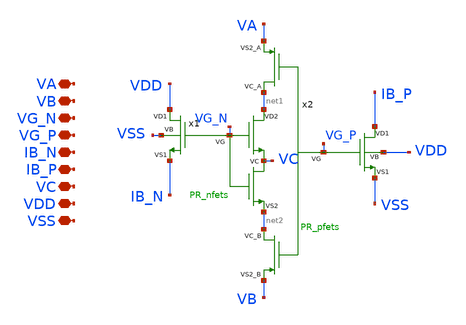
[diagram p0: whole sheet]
** sch_path: TIA/xschem/PseudoResistor/PR_net.sch
**.subckt PR_net VA VB VG_N VG_P IB_N IB_P VC VDD VSS
*.iopin VA
*.iopin VB
*.iopin VG_N
*.iopin VG_P
*.iopin IB_N
*.iopin IB_P
*.iopin VC
*.iopin VDD
*.iopin VSS
x1 VDD net1 IB_N net2 VG_N VC VSS PR_nfets
x2 IB_P VSS VA VB VG_P net1 net2 VDD PR_pfets
**.ends

* expanding   symbol:  /home/gmaranhao/Desktop/gf180_work/TIA/PseudoResistor/PR_nfets.sym # of
*+ pins=7
** sym_path: TIA/xschem/PseudoResistor/PR_nfets.sym
** sch_path: TIA/xschem/PseudoResistor/PR_nfets.sch
.subckt PR_nfets VD1 VD2 VS1 VS2 VG VC VB
*.iopin VD1
*.iopin VD2
*.iopin VS1
*.iopin VS2
*.iopin VG
*.iopin VC
*.iopin VB
XM5 VB VB VB VB nfet_03v3 L=2u W=2u nf=1 ad='int((nf+1)/2) * W/nf * 0.18u' as='int((nf+2)/2) * W/nf * 0.18u'
+ pd='2*int((nf+1)/2) * (W/nf + 0.18u)' ps='2*int((nf+2)/2) * (W/nf + 0.18u)' nrd='0.18u / W' nrs='0.18u / W'
+ sa=0 sb=0 sd=0 m=32
XM3 VD2 VG net1 VB nfet_03v3 L=2u W=2u nf=1 ad='int((nf+1)/2) * W/nf * 0.18u' as='int((nf+2)/2) * W/nf * 0.18u'
+ pd='2*int((nf+1)/2) * (W/nf + 0.18u)' ps='2*int((nf+2)/2) * (W/nf + 0.18u)' nrd='0.18u / W' nrs='0.18u / W'
+ sa=0 sb=0 sd=0 m=1
XM4 net1 VG VC VB nfet_03v3 L=2u W=2u nf=1 ad='int((nf+1)/2) * W/nf * 0.18u' as='int((nf+2)/2) * W/nf * 0.18u'
+ pd='2*int((nf+1)/2) * (W/nf + 0.18u)' ps='2*int((nf+2)/2) * (W/nf + 0.18u)' nrd='0.18u / W' nrs='0.18u / W'
+ sa=0 sb=0 sd=0 m=1
XM6 VD2 VG net2 VB nfet_03v3 L=2u W=2u nf=1 ad='int((nf+1)/2) * W/nf * 0.18u' as='int((nf+2)/2) * W/nf * 0.18u'
+ pd='2*int((nf+1)/2) * (W/nf + 0.18u)' ps='2*int((nf+2)/2) * (W/nf + 0.18u)' nrd='0.18u / W' nrs='0.18u / W'
+ sa=0 sb=0 sd=0 m=1
XM8 net2 VG VC VB nfet_03v3 L=2u W=2u nf=1 ad='int((nf+1)/2) * W/nf * 0.18u' as='int((nf+2)/2) * W/nf * 0.18u'
+ pd='2*int((nf+1)/2) * (W/nf + 0.18u)' ps='2*int((nf+2)/2) * (W/nf + 0.18u)' nrd='0.18u / W' nrs='0.18u / W'
+ sa=0 sb=0 sd=0 m=1
XM1 VC VG net3 VB nfet_03v3 L=2u W=2u nf=1 ad='int((nf+1)/2) * W/nf * 0.18u' as='int((nf+2)/2) * W/nf * 0.18u'
+ pd='2*int((nf+1)/2) * (W/nf + 0.18u)' ps='2*int((nf+2)/2) * (W/nf + 0.18u)' nrd='0.18u / W' nrs='0.18u / W'
+ sa=0 sb=0 sd=0 m=1
XM9 net3 VG VS2 VB nfet_03v3 L=2u W=2u nf=1 ad='int((nf+1)/2) * W/nf * 0.18u' as='int((nf+2)/2) * W/nf * 0.18u'
+ pd='2*int((nf+1)/2) * (W/nf + 0.18u)' ps='2*int((nf+2)/2) * (W/nf + 0.18u)' nrd='0.18u / W' nrs='0.18u / W'
+ sa=0 sb=0 sd=0 m=1
XM10 VC VG net4 VB nfet_03v3 L=2u W=2u nf=1 ad='int((nf+1)/2) * W/nf * 0.18u' as='int((nf+2)/2) * W/nf * 0.18u'
+ pd='2*int((nf+1)/2) * (W/nf + 0.18u)' ps='2*int((nf+2)/2) * (W/nf + 0.18u)' nrd='0.18u / W' nrs='0.18u / W'
+ sa=0 sb=0 sd=0 m=1
XM11 net4 VG VS2 VB nfet_03v3 L=2u W=2u nf=1 ad='int((nf+1)/2) * W/nf * 0.18u' as='int((nf+2)/2) * W/nf * 0.18u'
+ pd='2*int((nf+1)/2) * (W/nf + 0.18u)' ps='2*int((nf+2)/2) * (W/nf + 0.18u)' nrd='0.18u / W' nrs='0.18u / W'
+ sa=0 sb=0 sd=0 m=1
XM2 VD1 VG net5 VB nfet_03v3 L=2u W=2u nf=1 ad='int((nf+1)/2) * W/nf * 0.18u' as='int((nf+2)/2) * W/nf * 0.18u'
+ pd='2*int((nf+1)/2) * (W/nf + 0.18u)' ps='2*int((nf+2)/2) * (W/nf + 0.18u)' nrd='0.18u / W' nrs='0.18u / W'
+ sa=0 sb=0 sd=0 m=1
XM12 net5 VG VS1 VB nfet_03v3 L=2u W=2u nf=1 ad='int((nf+1)/2) * W/nf * 0.18u' as='int((nf+2)/2) * W/nf * 0.18u'
+ pd='2*int((nf+1)/2) * (W/nf + 0.18u)' ps='2*int((nf+2)/2) * (W/nf + 0.18u)' nrd='0.18u / W' nrs='0.18u / W'
+ sa=0 sb=0 sd=0 m=1
XM13 VD1 VG net6 VB nfet_03v3 L=2u W=2u nf=1 ad='int((nf+1)/2) * W/nf * 0.18u' as='int((nf+2)/2) * W/nf * 0.18u'
+ pd='2*int((nf+1)/2) * (W/nf + 0.18u)' ps='2*int((nf+2)/2) * (W/nf + 0.18u)' nrd='0.18u / W' nrs='0.18u / W'
+ sa=0 sb=0 sd=0 m=1
XM14 net6 VG VS1 VB nfet_03v3 L=2u W=2u nf=1 ad='int((nf+1)/2) * W/nf * 0.18u' as='int((nf+2)/2) * W/nf * 0.18u'
+ pd='2*int((nf+1)/2) * (W/nf + 0.18u)' ps='2*int((nf+2)/2) * (W/nf + 0.18u)' nrd='0.18u / W' nrs='0.18u / W'
+ sa=0 sb=0 sd=0 m=1
XM7 VD1 VG net7 VB nfet_03v3 L=2u W=2u nf=1 ad='int((nf+1)/2) * W/nf * 0.18u' as='int((nf+2)/2) * W/nf * 0.18u'
+ pd='2*int((nf+1)/2) * (W/nf + 0.18u)' ps='2*int((nf+2)/2) * (W/nf + 0.18u)' nrd='0.18u / W' nrs='0.18u / W'
+ sa=0 sb=0 sd=0 m=1
XM15 net7 VG VS1 VB nfet_03v3 L=2u W=2u nf=1 ad='int((nf+1)/2) * W/nf * 0.18u' as='int((nf+2)/2) * W/nf * 0.18u'
+ pd='2*int((nf+1)/2) * (W/nf + 0.18u)' ps='2*int((nf+2)/2) * (W/nf + 0.18u)' nrd='0.18u / W' nrs='0.18u / W'
+ sa=0 sb=0 sd=0 m=1
XM16 VD1 VG net8 VB nfet_03v3 L=2u W=2u nf=1 ad='int((nf+1)/2) * W/nf * 0.18u' as='int((nf+2)/2) * W/nf * 0.18u'
+ pd='2*int((nf+1)/2) * (W/nf + 0.18u)' ps='2*int((nf+2)/2) * (W/nf + 0.18u)' nrd='0.18u / W' nrs='0.18u / W'
+ sa=0 sb=0 sd=0 m=1
XM17 net8 VG VS1 VB nfet_03v3 L=2u W=2u nf=1 ad='int((nf+1)/2) * W/nf * 0.18u' as='int((nf+2)/2) * W/nf * 0.18u'
+ pd='2*int((nf+1)/2) * (W/nf + 0.18u)' ps='2*int((nf+2)/2) * (W/nf + 0.18u)' nrd='0.18u / W' nrs='0.18u / W'
+ sa=0 sb=0 sd=0 m=1
.ends


* expanding   symbol:  /home/gmaranhao/Desktop/gf180_work/TIA/PseudoResistor/PR_pfets.sym # of
*+ pins=8
** sym_path: TIA/xschem/PseudoResistor/PR_pfets.sym
** sch_path: TIA/xschem/PseudoResistor/PR_pfets.sch
.subckt PR_pfets VD1 VS1 VS2_A VS2_B VG VC_A VC_B VB
*.iopin VD1
*.iopin VS1
*.iopin VS2_A
*.iopin VS2_B
*.iopin VG
*.iopin VC_A
*.iopin VC_B
*.iopin VB
XM1 net3 VG VS1 VB pfet_03v3 L=2u W=2u nf=1 ad='int((nf+1)/2) * W/nf * 0.18u' as='int((nf+2)/2) * W/nf * 0.18u'
+ pd='2*int((nf+1)/2) * (W/nf + 0.18u)' ps='2*int((nf+2)/2) * (W/nf + 0.18u)' nrd='0.18u / W' nrs='0.18u / W'
+ sa=0 sb=0 sd=0 m=1
XM2 VD1 VG net3 VB pfet_03v3 L=2u W=2u nf=1 ad='int((nf+1)/2) * W/nf * 0.18u' as='int((nf+2)/2) * W/nf * 0.18u'
+ pd='2*int((nf+1)/2) * (W/nf + 0.18u)' ps='2*int((nf+2)/2) * (W/nf + 0.18u)' nrd='0.18u / W' nrs='0.18u / W'
+ sa=0 sb=0 sd=0 m=1
XM5 net4 VG VS1 VB pfet_03v3 L=2u W=2u nf=1 ad='int((nf+1)/2) * W/nf * 0.18u' as='int((nf+2)/2) * W/nf * 0.18u'
+ pd='2*int((nf+1)/2) * (W/nf + 0.18u)' ps='2*int((nf+2)/2) * (W/nf + 0.18u)' nrd='0.18u / W' nrs='0.18u / W'
+ sa=0 sb=0 sd=0 m=1
XM6 VD1 VG net4 VB pfet_03v3 L=2u W=2u nf=1 ad='int((nf+1)/2) * W/nf * 0.18u' as='int((nf+2)/2) * W/nf * 0.18u'
+ pd='2*int((nf+1)/2) * (W/nf + 0.18u)' ps='2*int((nf+2)/2) * (W/nf + 0.18u)' nrd='0.18u / W' nrs='0.18u / W'
+ sa=0 sb=0 sd=0 m=1
XM7 net5 VG VS1 VB pfet_03v3 L=2u W=2u nf=1 ad='int((nf+1)/2) * W/nf * 0.18u' as='int((nf+2)/2) * W/nf * 0.18u'
+ pd='2*int((nf+1)/2) * (W/nf + 0.18u)' ps='2*int((nf+2)/2) * (W/nf + 0.18u)' nrd='0.18u / W' nrs='0.18u / W'
+ sa=0 sb=0 sd=0 m=1
XM9 VD1 VG net5 VB pfet_03v3 L=2u W=2u nf=1 ad='int((nf+1)/2) * W/nf * 0.18u' as='int((nf+2)/2) * W/nf * 0.18u'
+ pd='2*int((nf+1)/2) * (W/nf + 0.18u)' ps='2*int((nf+2)/2) * (W/nf + 0.18u)' nrd='0.18u / W' nrs='0.18u / W'
+ sa=0 sb=0 sd=0 m=1
XM10 net6 VG VS1 VB pfet_03v3 L=2u W=2u nf=1 ad='int((nf+1)/2) * W/nf * 0.18u' as='int((nf+2)/2) * W/nf * 0.18u'
+ pd='2*int((nf+1)/2) * (W/nf + 0.18u)' ps='2*int((nf+2)/2) * (W/nf + 0.18u)' nrd='0.18u / W' nrs='0.18u / W'
+ sa=0 sb=0 sd=0 m=1
XM11 VD1 VG net6 VB pfet_03v3 L=2u W=2u nf=1 ad='int((nf+1)/2) * W/nf * 0.18u' as='int((nf+2)/2) * W/nf * 0.18u'
+ pd='2*int((nf+1)/2) * (W/nf + 0.18u)' ps='2*int((nf+2)/2) * (W/nf + 0.18u)' nrd='0.18u / W' nrs='0.18u / W'
+ sa=0 sb=0 sd=0 m=1
XM12 net1 VG VS2_A VB pfet_03v3 L=2u W=2u nf=1 ad='int((nf+1)/2) * W/nf * 0.18u' as='int((nf+2)/2) * W/nf * 0.18u'
+ pd='2*int((nf+1)/2) * (W/nf + 0.18u)' ps='2*int((nf+2)/2) * (W/nf + 0.18u)' nrd='0.18u / W' nrs='0.18u / W'
+ sa=0 sb=0 sd=0 m=1
XM13 VC_A VG net1 VB pfet_03v3 L=2u W=2u nf=1 ad='int((nf+1)/2) * W/nf * 0.18u' as='int((nf+2)/2) * W/nf * 0.18u'
+ pd='2*int((nf+1)/2) * (W/nf + 0.18u)' ps='2*int((nf+2)/2) * (W/nf + 0.18u)' nrd='0.18u / W' nrs='0.18u / W'
+ sa=0 sb=0 sd=0 m=1
XM14 net2 VG VS2_A VB pfet_03v3 L=2u W=2u nf=1 ad='int((nf+1)/2) * W/nf * 0.18u' as='int((nf+2)/2) * W/nf * 0.18u'
+ pd='2*int((nf+1)/2) * (W/nf + 0.18u)' ps='2*int((nf+2)/2) * (W/nf + 0.18u)' nrd='0.18u / W' nrs='0.18u / W'
+ sa=0 sb=0 sd=0 m=1
XM15 VC_A VG net2 VB pfet_03v3 L=2u W=2u nf=1 ad='int((nf+1)/2) * W/nf * 0.18u' as='int((nf+2)/2) * W/nf * 0.18u'
+ pd='2*int((nf+1)/2) * (W/nf + 0.18u)' ps='2*int((nf+2)/2) * (W/nf + 0.18u)' nrd='0.18u / W' nrs='0.18u / W'
+ sa=0 sb=0 sd=0 m=1
XM16 VC_B VG net7 VB pfet_03v3 L=2u W=2u nf=1 ad='int((nf+1)/2) * W/nf * 0.18u' as='int((nf+2)/2) * W/nf * 0.18u'
+ pd='2*int((nf+1)/2) * (W/nf + 0.18u)' ps='2*int((nf+2)/2) * (W/nf + 0.18u)' nrd='0.18u / W' nrs='0.18u / W'
+ sa=0 sb=0 sd=0 m=1
XM17 net7 VG VS2_B VB pfet_03v3 L=2u W=2u nf=1 ad='int((nf+1)/2) * W/nf * 0.18u' as='int((nf+2)/2) * W/nf * 0.18u'
+ pd='2*int((nf+1)/2) * (W/nf + 0.18u)' ps='2*int((nf+2)/2) * (W/nf + 0.18u)' nrd='0.18u / W' nrs='0.18u / W'
+ sa=0 sb=0 sd=0 m=1
XM18 VC_B VG net8 VB pfet_03v3 L=2u W=2u nf=1 ad='int((nf+1)/2) * W/nf * 0.18u' as='int((nf+2)/2) * W/nf * 0.18u'
+ pd='2*int((nf+1)/2) * (W/nf + 0.18u)' ps='2*int((nf+2)/2) * (W/nf + 0.18u)' nrd='0.18u / W' nrs='0.18u / W'
+ sa=0 sb=0 sd=0 m=1
XM19 net8 VG VS2_B VB pfet_03v3 L=2u W=2u nf=1 ad='int((nf+1)/2) * W/nf * 0.18u' as='int((nf+2)/2) * W/nf * 0.18u'
+ pd='2*int((nf+1)/2) * (W/nf + 0.18u)' ps='2*int((nf+2)/2) * (W/nf + 0.18u)' nrd='0.18u / W' nrs='0.18u / W'
+ sa=0 sb=0 sd=0 m=1
XM3 VB VB VB VB pfet_03v3 L=2u W=2u nf=1 ad='int((nf+1)/2) * W/nf * 0.18u' as='int((nf+2)/2) * W/nf * 0.18u'
+ pd='2*int((nf+1)/2) * (W/nf + 0.18u)' ps='2*int((nf+2)/2) * (W/nf + 0.18u)' nrd='0.18u / W' nrs='0.18u / W'
+ sa=0 sb=0 sd=0 m=32
.ends

.end
